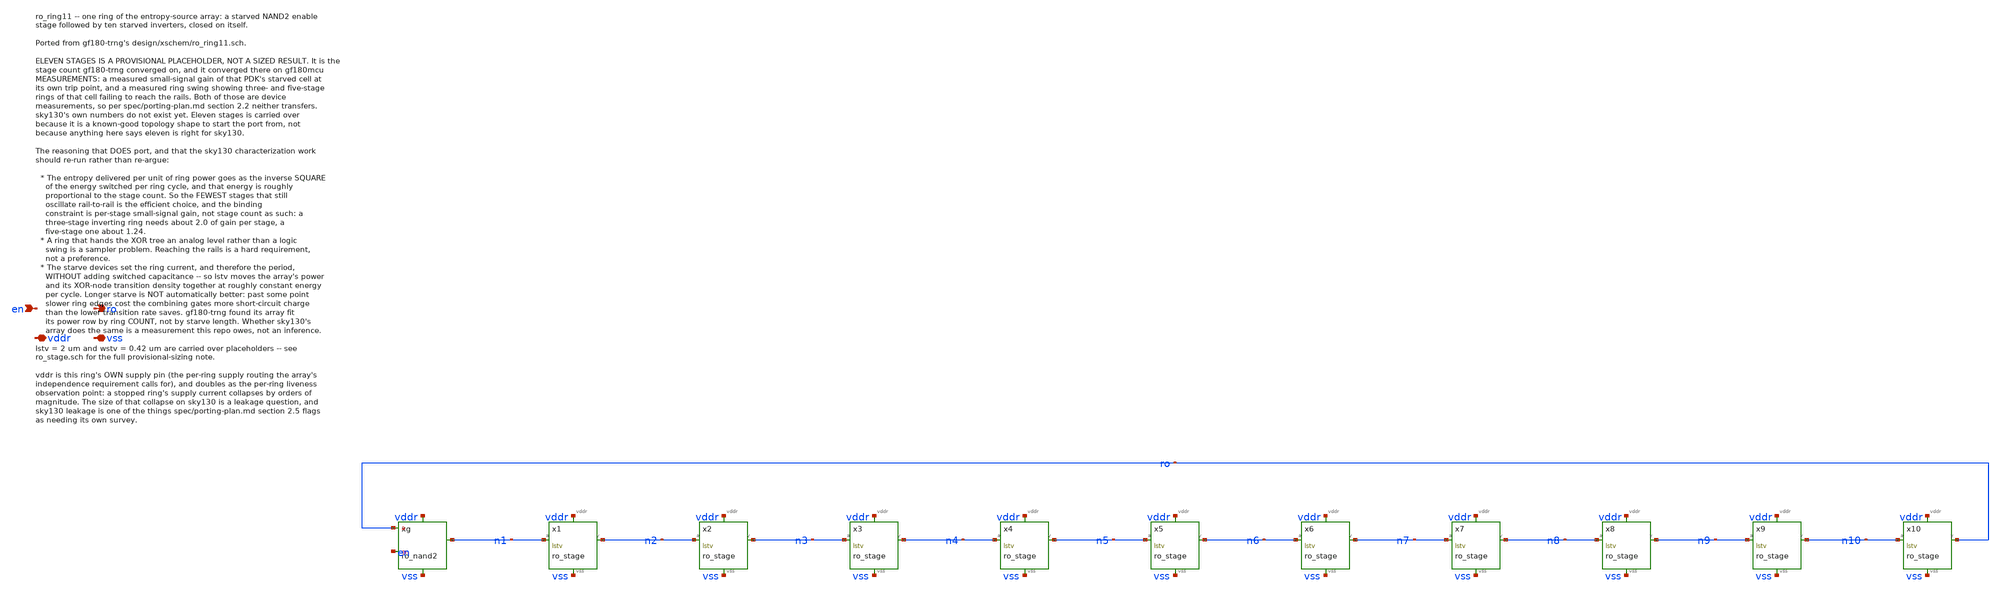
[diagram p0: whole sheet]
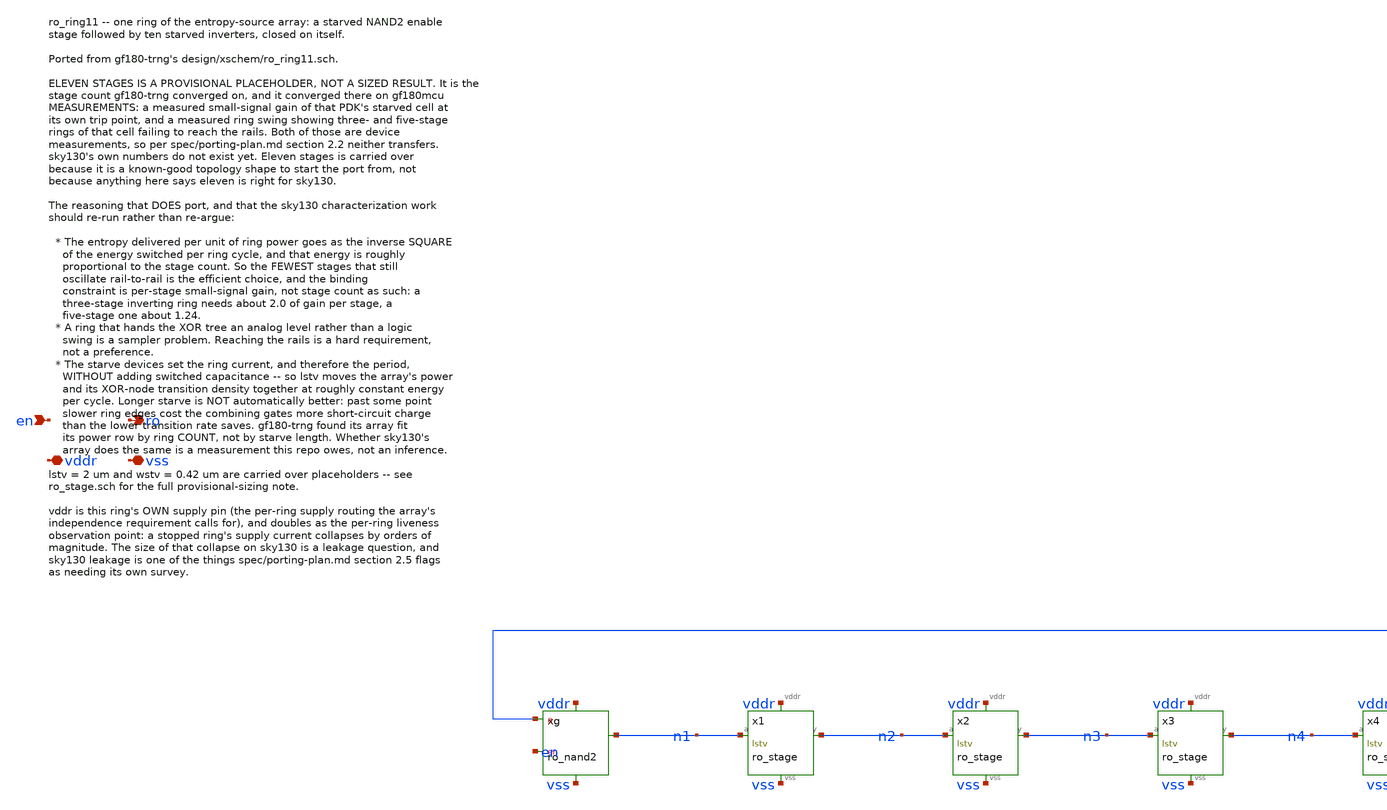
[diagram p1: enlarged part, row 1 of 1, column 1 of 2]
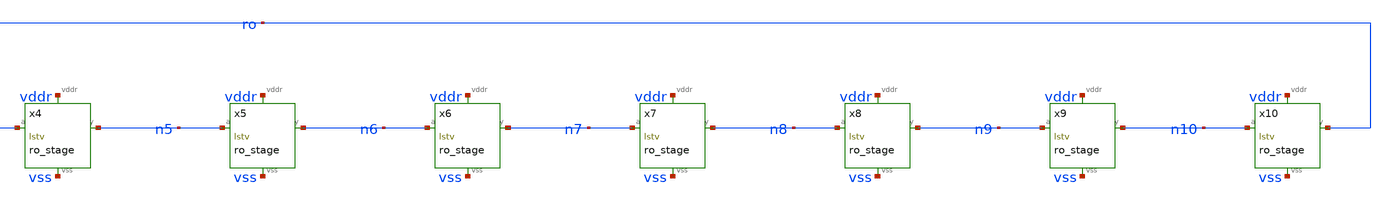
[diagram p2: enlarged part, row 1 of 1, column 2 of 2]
** sch_path: design/xschem/ro_ring11.sch
**.subckt ro_ring11 en ro vddr vss
*.ipin en
*.opin ro
*.iopin vddr
*.iopin vss
xg ro en n1 vddr vss ro_nand2 wstv=wstv lstv=lstv cld=cld
x1 n1 n2 vddr vss ro_stage wstv=wstv lstv=lstv cld=cld
x2 n2 n3 vddr vss ro_stage wstv=wstv lstv=lstv cld=cld
x3 n3 n4 vddr vss ro_stage wstv=wstv lstv=lstv cld=cld
x4 n4 n5 vddr vss ro_stage wstv=wstv lstv=lstv cld=cld
x5 n5 n6 vddr vss ro_stage wstv=wstv lstv=lstv cld=cld
x6 n6 n7 vddr vss ro_stage wstv=wstv lstv=lstv cld=cld
x7 n7 n8 vddr vss ro_stage wstv=wstv lstv=lstv cld=cld
x8 n8 n9 vddr vss ro_stage wstv=wstv lstv=lstv cld=cld
x9 n9 n10 vddr vss ro_stage wstv=wstv lstv=lstv cld=cld
x10 n10 ro vddr vss ro_stage wstv=wstv lstv=lstv cld=cld
**.ends

* expanding   symbol:  ro_nand2.sym # of pins=5
** sym_path: design/xschem/ro_nand2.sym
** sch_path: design/xschem/ro_nand2.sch
.subckt ro_nand2 a en y vddr vss  wstv=0.42 lstv=2 cld=0.5f
*.ipin a
*.ipin en
*.opin y
*.iopin vddr
*.iopin vss
XMph py vss vddr vddr sky130_fd_pr__pfet_01v8 L=lstv W=wstv nf=1 ad='int((nf+1)/2) * W/nf * 0.29' as='int((nf+2)/2) * W/nf * 0.29'
+ pd='2*int((nf+1)/2) * (W/nf + 0.29)' ps='2*int((nf+2)/2) * (W/nf + 0.29)' nrd='0.29 / W' nrs='0.29 / W'
+ sa=0 sb=0 sd=0 mult=1 m=1
XMpa y a py vddr sky130_fd_pr__pfet_01v8 L=0.15 W=0.84 nf=1 ad='int((nf+1)/2) * W/nf * 0.29' as='int((nf+2)/2) * W/nf * 0.29'
+ pd='2*int((nf+1)/2) * (W/nf + 0.29)' ps='2*int((nf+2)/2) * (W/nf + 0.29)' nrd='0.29 / W' nrs='0.29 / W'
+ sa=0 sb=0 sd=0 mult=1 m=1
XMpb y en py vddr sky130_fd_pr__pfet_01v8 L=0.15 W=0.84 nf=1 ad='int((nf+1)/2) * W/nf * 0.29' as='int((nf+2)/2) * W/nf * 0.29'
+ pd='2*int((nf+1)/2) * (W/nf + 0.29)' ps='2*int((nf+2)/2) * (W/nf + 0.29)' nrd='0.29 / W' nrs='0.29 / W'
+ sa=0 sb=0 sd=0 mult=1 m=1
XMna y a nm vss sky130_fd_pr__nfet_01v8 L=0.15 W=0.84 nf=1 ad='int((1 + 1)/2) * 0.84 / 1 * 0.29' as='int((1 + 2)/2) * 0.84 / 1 * 0.29'
+ pd='2*int((1 + 1)/2) * (0.84 / 1 + 0.29)' ps='2*int((1 + 2)/2) * (0.84 / 1 + 0.29)' nrd='0.29 / 0.84 '
+ nrs='0.29 / 0.84 ' sa=0 sb=0 sd=0 mult=1 m=1
XMnb nm en ny vss sky130_fd_pr__nfet_01v8 L=0.15 W=0.84 nf=1 ad='int((1 + 1)/2) * 0.84 / 1 * 0.29' as='int((1 + 2)/2) * 0.84 / 1 * 0.29'
+ pd='2*int((1 + 1)/2) * (0.84 / 1 + 0.29)' ps='2*int((1 + 2)/2) * (0.84 / 1 + 0.29)' nrd='0.29 / 0.84 '
+ nrs='0.29 / 0.84 ' sa=0 sb=0 sd=0 mult=1 m=1
XMnt ny vddr vss vss sky130_fd_pr__nfet_01v8 L=lstv W=wstv nf=1 ad='int((1 + 1)/2) * wstv / 1 * 0.29'
+ as='int((1 + 2)/2) * wstv / 1 * 0.29' pd='2*int((1 + 1)/2) * (wstv / 1 + 0.29)' ps='2*int((1 + 2)/2) * (wstv / 1 + 0.29)'
+ nrd='0.29 / wstv ' nrs='0.29 / wstv ' sa=0 sb=0 sd=0 mult=1 m=1
Cld y vss 'cld' m=1
.ends


* expanding   symbol:  ro_stage.sym # of pins=4
** sym_path: design/xschem/ro_stage.sym
** sch_path: design/xschem/ro_stage.sch
.subckt ro_stage a y vddr vss  wstv=0.42 lstv=2 cld=0.5f
*.ipin a
*.opin y
*.iopin vddr
*.iopin vss
XMph py vss vddr vddr sky130_fd_pr__pfet_01v8 L=lstv W=wstv nf=1 ad='int((nf+1)/2) * W/nf * 0.29' as='int((nf+2)/2) * W/nf * 0.29'
+ pd='2*int((nf+1)/2) * (W/nf + 0.29)' ps='2*int((nf+2)/2) * (W/nf + 0.29)' nrd='0.29 / W' nrs='0.29 / W'
+ sa=0 sb=0 sd=0 mult=1 m=1
XMp y a py vddr sky130_fd_pr__pfet_01v8 L=0.15 W=0.84 nf=1 ad='int((nf+1)/2) * W/nf * 0.29' as='int((nf+2)/2) * W/nf * 0.29'
+ pd='2*int((nf+1)/2) * (W/nf + 0.29)' ps='2*int((nf+2)/2) * (W/nf + 0.29)' nrd='0.29 / W' nrs='0.29 / W'
+ sa=0 sb=0 sd=0 mult=1 m=1
XMn y a ny vss sky130_fd_pr__nfet_01v8 L=0.15 W=0.42 nf=1 ad='int((1 + 1)/2) * 0.42 / 1 * 0.29' as='int((1 + 2)/2) * 0.42 / 1 * 0.29'
+ pd='2*int((1 + 1)/2) * (0.42 / 1 + 0.29)' ps='2*int((1 + 2)/2) * (0.42 / 1 + 0.29)' nrd='0.29 / 0.42 '
+ nrs='0.29 / 0.42 ' sa=0 sb=0 sd=0 mult=1 m=1
XMnt ny vddr vss vss sky130_fd_pr__nfet_01v8 L=lstv W=wstv nf=1 ad='int((1 + 1)/2) * wstv / 1 * 0.29'
+ as='int((1 + 2)/2) * wstv / 1 * 0.29' pd='2*int((1 + 1)/2) * (wstv / 1 + 0.29)' ps='2*int((1 + 2)/2) * (wstv / 1 + 0.29)'
+ nrd='0.29 / wstv ' nrs='0.29 / wstv ' sa=0 sb=0 sd=0 mult=1 m=1
Cld y vss 'cld' m=1
.ends

.end
